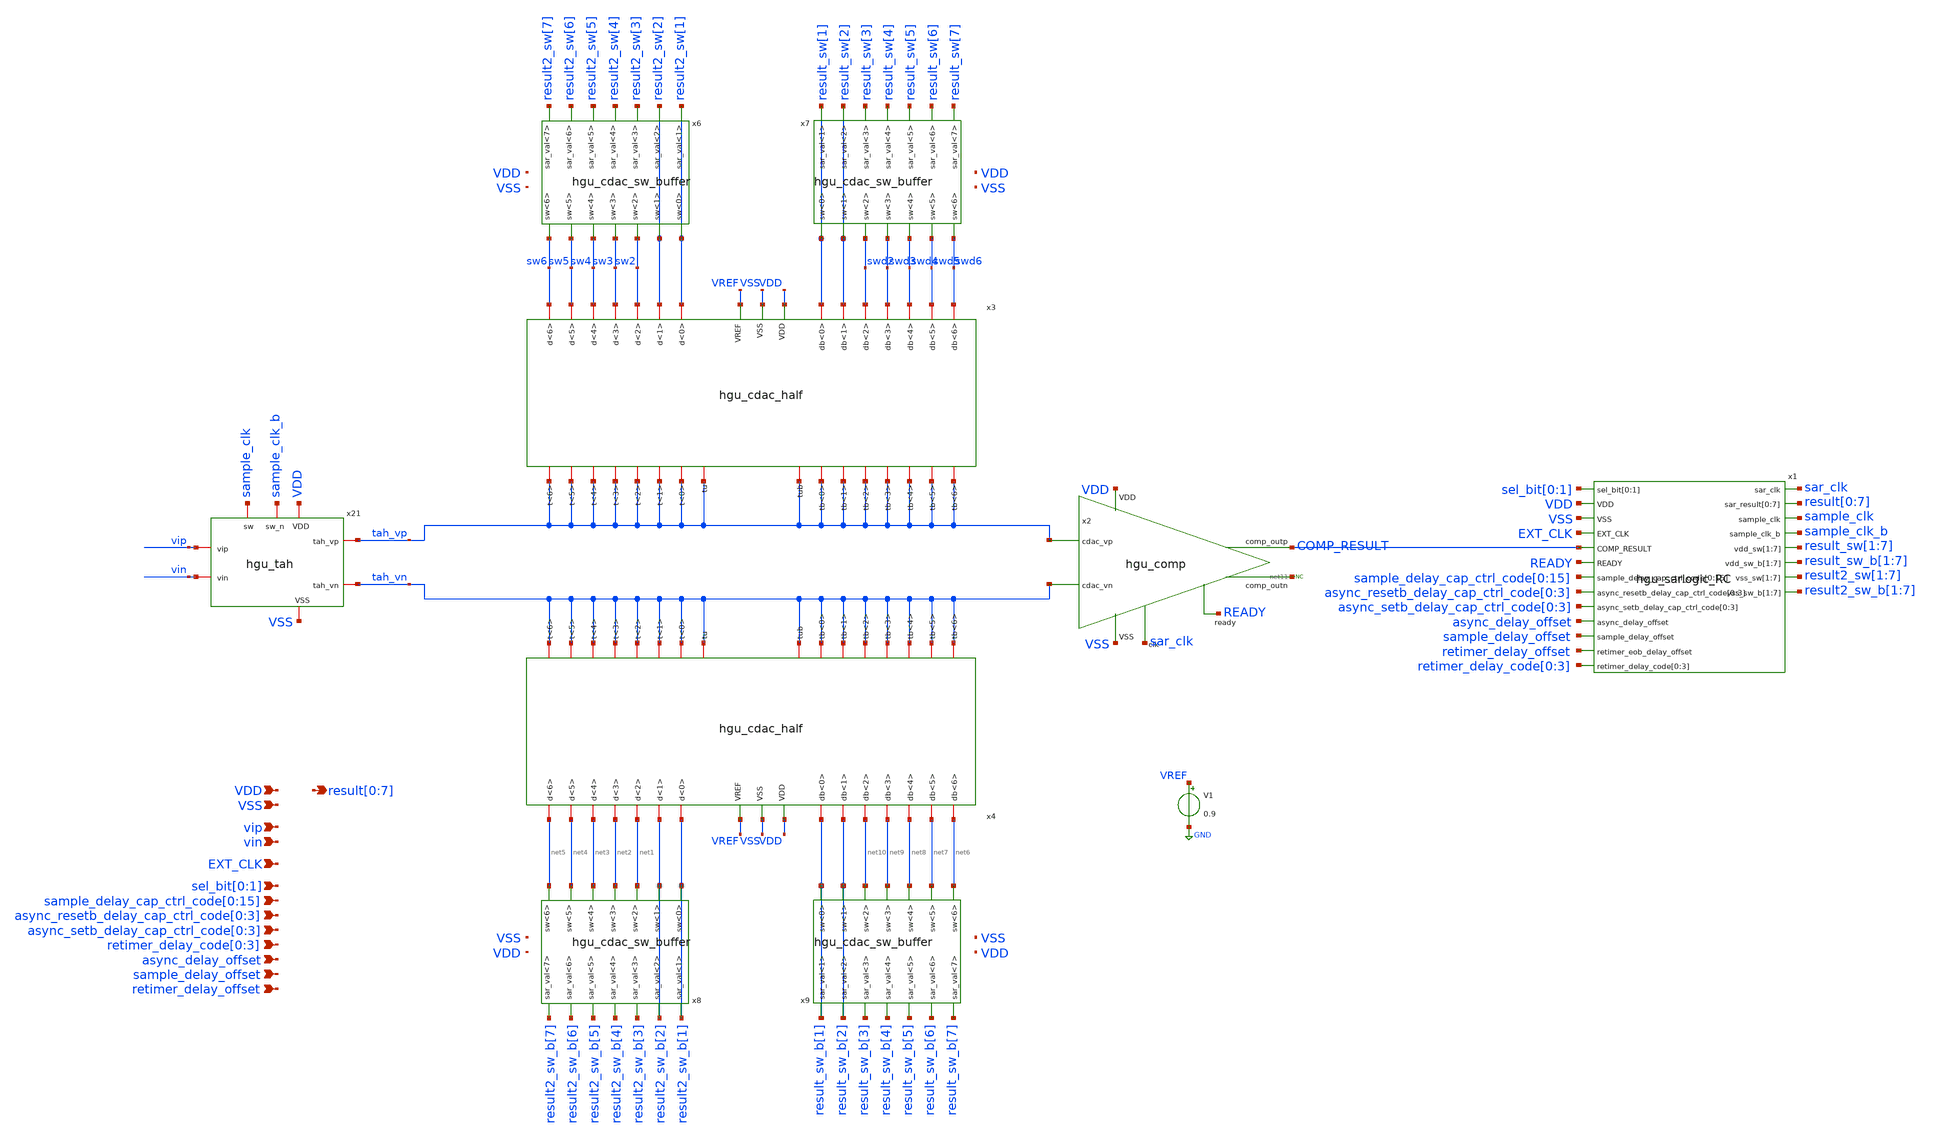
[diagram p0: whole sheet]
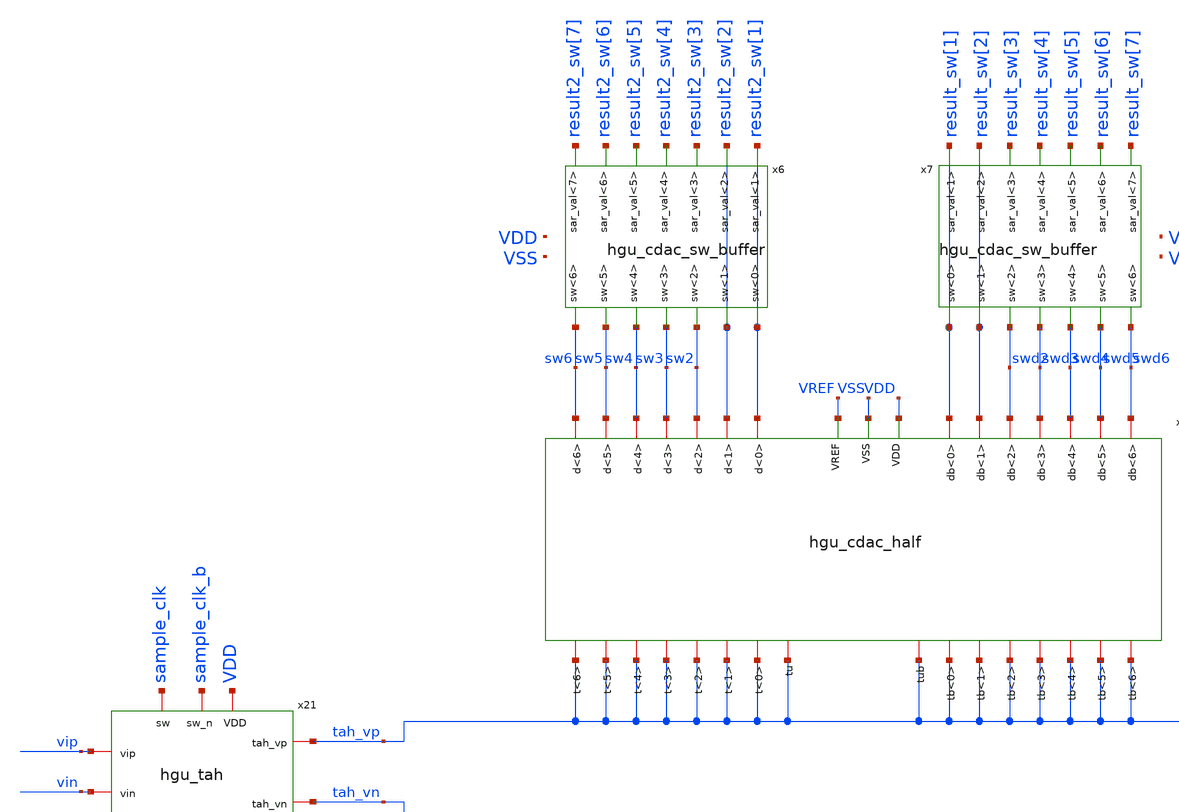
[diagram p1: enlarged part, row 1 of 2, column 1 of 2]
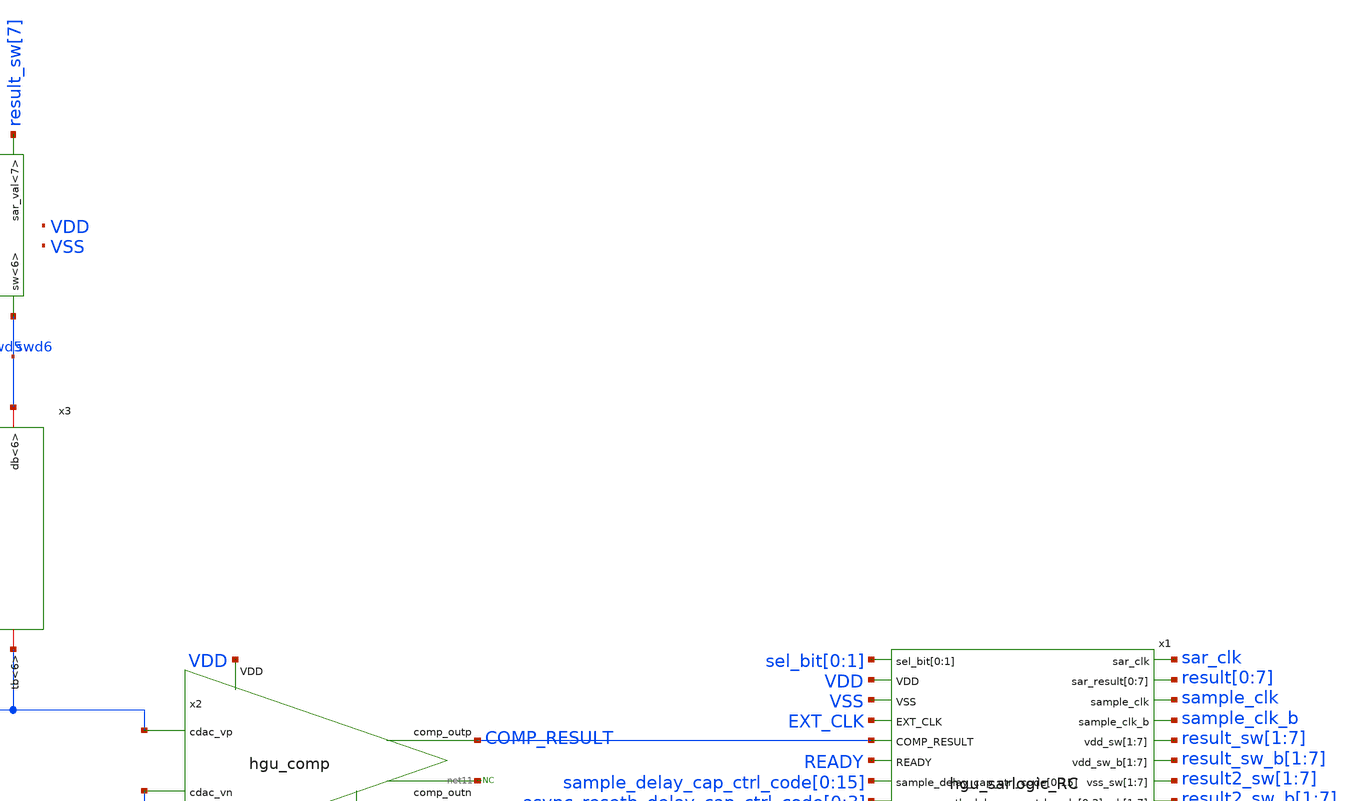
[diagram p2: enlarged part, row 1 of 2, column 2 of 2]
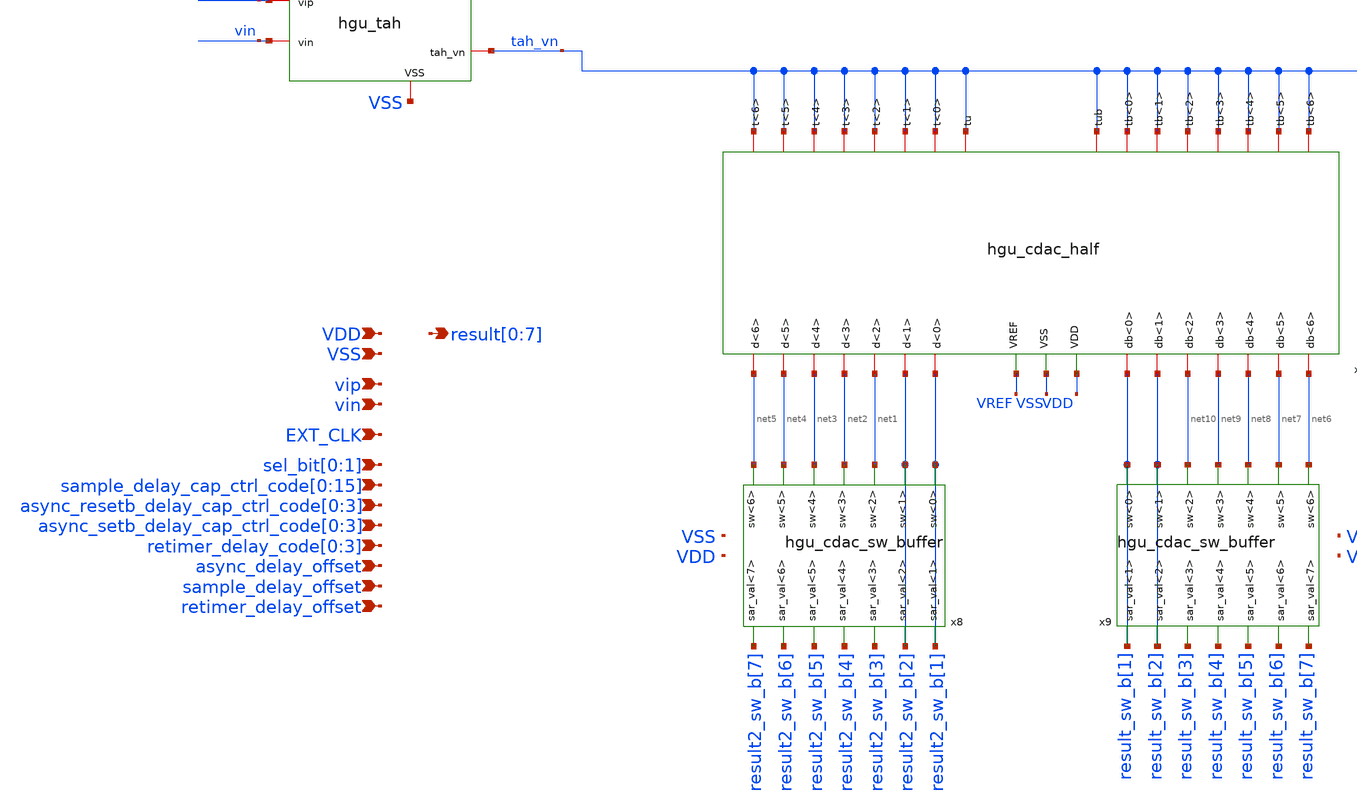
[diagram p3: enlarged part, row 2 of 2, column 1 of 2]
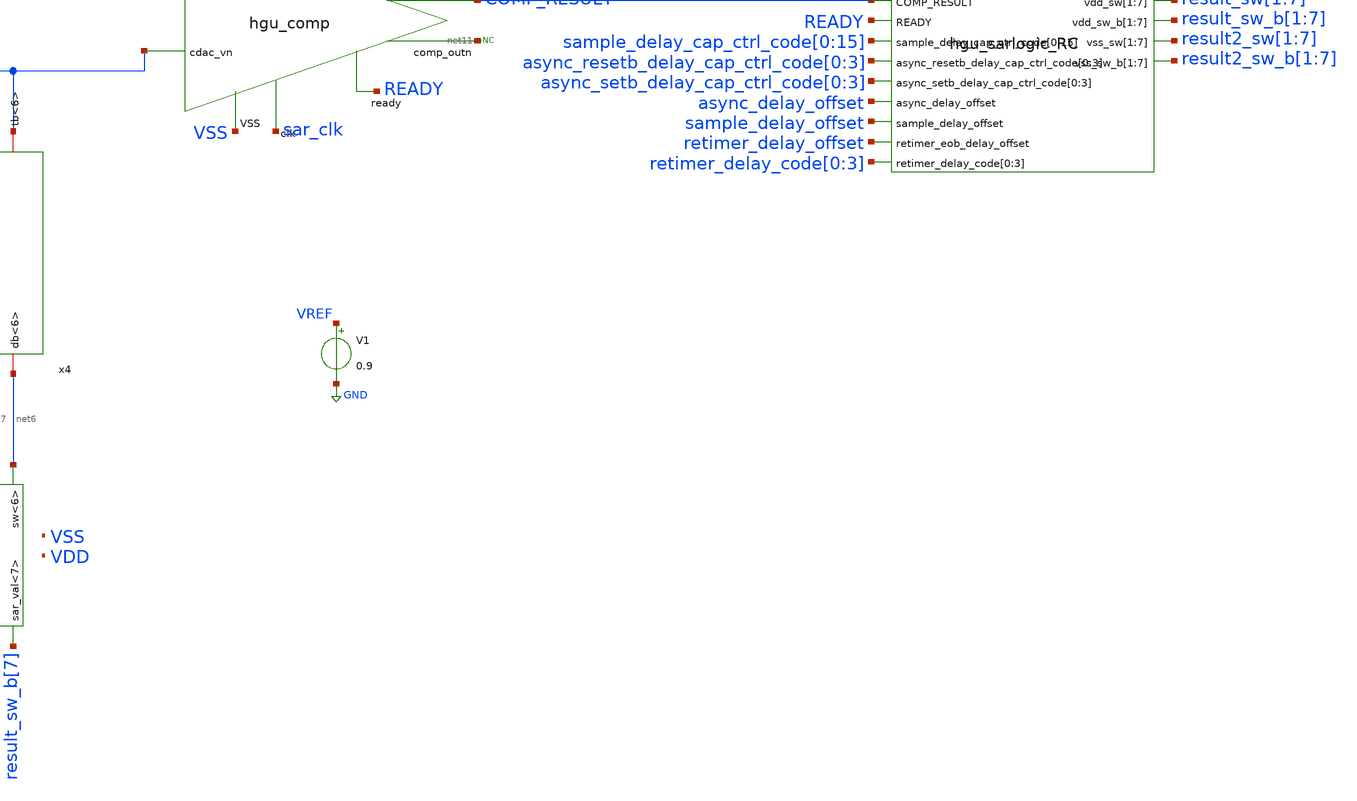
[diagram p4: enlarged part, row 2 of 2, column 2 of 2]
** sch_path: hgu/xschem/hgu_top_block.sch
**.subckt hgu_top_block VDD VSS
*+ result[0],result[1],result[2],result[3],result[4],result[5],result[6],result[7] EXT_CLK vip vin sel_bit[0],sel_bit[1]
*+ sample_delay_cap_ctrl_code[0],sample_delay_cap_ctrl_code[1],sample_delay_cap_ctrl_code[2],sample_delay_cap_ctrl_code[3],sample_delay_cap_ctrl_code[4],sample_delay_cap_ctrl_code[5],sample_delay_cap_ctrl_code[6],sample_delay_cap_ctrl_code[7],sample_delay_cap_ctrl_code[8],sample_delay_cap_ctrl_code[9],sample_delay_cap_ctrl_code[10],sample_delay_cap_ctrl_code[11],sample_delay_cap_ctrl_code[12],sample_delay_cap_ctrl_code[13],sample_delay_cap_ctrl_code[14],sample_delay_cap_ctrl_code[15]
*+ async_resetb_delay_cap_ctrl_code[0],async_resetb_delay_cap_ctrl_code[1],async_resetb_delay_cap_ctrl_code[2],async_resetb_delay_cap_ctrl_code[3]
*+ async_setb_delay_cap_ctrl_code[0],async_setb_delay_cap_ctrl_code[1],async_setb_delay_cap_ctrl_code[2],async_setb_delay_cap_ctrl_code[3] async_delay_offset sample_delay_offset
*+ retimer_delay_code[0],retimer_delay_code[1],retimer_delay_code[2],retimer_delay_code[3] retimer_delay_offset
*.ipin VDD
*.ipin VSS
*.opin result[0],result[1],result[2],result[3],result[4],result[5],result[6],result[7]
*.ipin EXT_CLK
*.ipin vip
*.ipin vin
*.ipin sel_bit[0],sel_bit[1]
*.ipin
*+ sample_delay_cap_ctrl_code[0],sample_delay_cap_ctrl_code[1],sample_delay_cap_ctrl_code[2],sample_delay_cap_ctrl_code[3],sample_delay_cap_ctrl_code[4],sample_delay_cap_ctrl_code[5],sample_delay_cap_ctrl_code[6],sample_delay_cap_ctrl_code[7],sample_delay_cap_ctrl_code[8],sample_delay_cap_ctrl_code[9],sample_delay_cap_ctrl_code[10],sample_delay_cap_ctrl_code[11],sample_delay_cap_ctrl_code[12],sample_delay_cap_ctrl_code[13],sample_delay_cap_ctrl_code[14],sample_delay_cap_ctrl_code[15]
*.ipin
*+ async_resetb_delay_cap_ctrl_code[0],async_resetb_delay_cap_ctrl_code[1],async_resetb_delay_cap_ctrl_code[2],async_resetb_delay_cap_ctrl_code[3]
*.ipin
*+ async_setb_delay_cap_ctrl_code[0],async_setb_delay_cap_ctrl_code[1],async_setb_delay_cap_ctrl_code[2],async_setb_delay_cap_ctrl_code[3]
*.ipin async_delay_offset
*.ipin sample_delay_offset
*.ipin retimer_delay_code[0],retimer_delay_code[1],retimer_delay_code[2],retimer_delay_code[3]
*.ipin retimer_delay_offset
x1 sar_clk result[0] result[1] result[2] result[3] result[4] result[5] result[6] result[7]
+ sample_clk sel_bit[0] sel_bit[1] sample_clk_b VDD VSS EXT_CLK COMP_RESULT result_sw[1] result_sw[2]
+ result_sw[3] result_sw[4] result_sw[5] result_sw[6] result_sw[7] READY result_sw_b[1] result_sw_b[2]
+ result_sw_b[3] result_sw_b[4] result_sw_b[5] result_sw_b[6] result_sw_b[7] result2_sw[1] result2_sw[2]
+ result2_sw[3] result2_sw[4] result2_sw[5] result2_sw[6] result2_sw[7] result2_sw_b[1] result2_sw_b[2]
+ result2_sw_b[3] result2_sw_b[4] result2_sw_b[5] result2_sw_b[6] result2_sw_b[7] sample_delay_cap_ctrl_code[0]
+ sample_delay_cap_ctrl_code[1] sample_delay_cap_ctrl_code[2] sample_delay_cap_ctrl_code[3] sample_delay_cap_ctrl_code[4]
+ sample_delay_cap_ctrl_code[5] sample_delay_cap_ctrl_code[6] sample_delay_cap_ctrl_code[7] sample_delay_cap_ctrl_code[8]
+ sample_delay_cap_ctrl_code[9] sample_delay_cap_ctrl_code[10] sample_delay_cap_ctrl_code[11] sample_delay_cap_ctrl_code[12]
+ sample_delay_cap_ctrl_code[13] sample_delay_cap_ctrl_code[14] sample_delay_cap_ctrl_code[15] async_resetb_delay_cap_ctrl_code[0]
+ async_resetb_delay_cap_ctrl_code[1] async_resetb_delay_cap_ctrl_code[2] async_resetb_delay_cap_ctrl_code[3]
+ async_setb_delay_cap_ctrl_code[0] async_setb_delay_cap_ctrl_code[1] async_setb_delay_cap_ctrl_code[2]
+ async_setb_delay_cap_ctrl_code[3] async_delay_offset sample_delay_offset retimer_delay_offset retimer_delay_code[0]
+ retimer_delay_code[1] retimer_delay_code[2] retimer_delay_code[3] hgu_sarlogic_RC
x2 READY tah_vn COMP_RESULT net11 tah_vp sar_clk VDD VSS hgu_comp
x3 sw5 swd4 sw3 result_sw[2] swd2 sw2 swd6 swd5 result_sw[1] sw4 sw6 result2_sw[2] result2_sw[1]
+ swd3 VSS VREF tah_vp tah_vp tah_vp tah_vp tah_vp tah_vp tah_vp tah_vp tah_vp tah_vp tah_vp tah_vp tah_vp
+ tah_vp tah_vp tah_vp VDD hgu_cdac_half
x4 net4 net8 net2 result_sw_b[2] net10 net1 net6 net7 result_sw_b[1] net3 net5 result2_sw_b[2]
+ result2_sw_b[1] net9 VSS VREF tah_vn tah_vn tah_vn tah_vn tah_vn tah_vn tah_vn tah_vn tah_vn tah_vn tah_vn tah_vn
+ tah_vn tah_vn tah_vn tah_vn VDD hgu_cdac_half
x21 sample_clk VDD VSS sample_clk_b tah_vp vip vin tah_vn hgu_tah
* noconn #net11
x6 result2_sw[3] result2_sw[6] result2_sw[1] result2_sw[2] result2_sw[4] result2_sw[5] result2_sw[7]
+ result2_sw[2] sw2 sw5 sw3 result2_sw[1] sw4 sw6 hgu_cdac_sw_buffer
x7 result_sw[3] result_sw[6] result_sw[1] result_sw[2] result_sw[4] result_sw[5] result_sw[7]
+ result_sw[2] swd2 swd5 swd3 result_sw[1] swd4 swd6 hgu_cdac_sw_buffer
x8 result2_sw_b[3] result2_sw_b[6] result2_sw_b[1] result2_sw_b[2] result2_sw_b[4] result2_sw_b[5]
+ result2_sw_b[7] result2_sw_b[2] net1 net4 net2 result2_sw_b[1] net3 net5 hgu_cdac_sw_buffer
x9 result_sw_b[3] result_sw_b[6] result_sw_b[1] result_sw_b[2] result_sw_b[4] result_sw_b[5]
+ result_sw_b[7] result_sw_b[2] net10 net7 net9 result_sw_b[1] net8 net6 hgu_cdac_sw_buffer
V1 VREF GND 0.9
**.ends
.GLOBAL GND
.end
